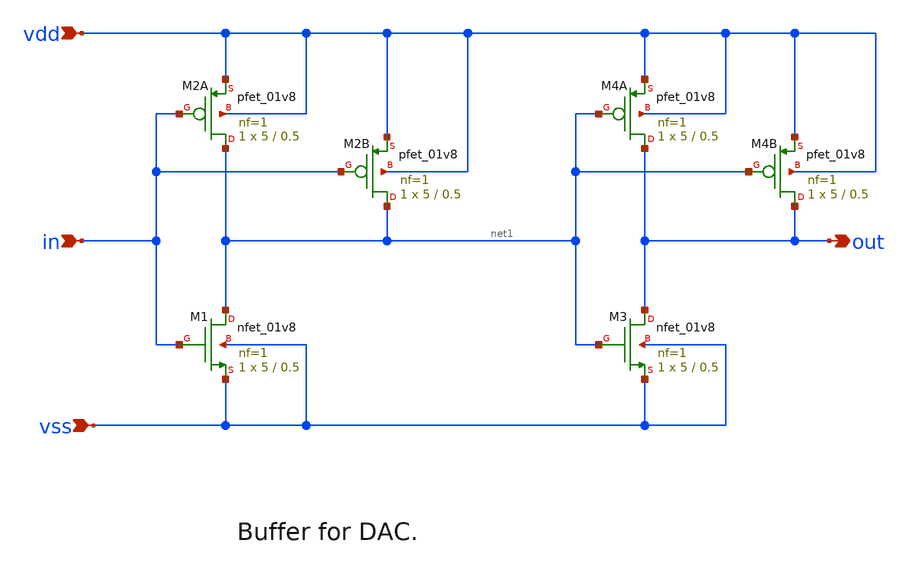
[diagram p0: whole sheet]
** sch_path: examples/3b_DAC_AMS/xschem/dac_drv.sch
**.subckt dac_drv vdd vss in out
*.ipin vdd
*.ipin vss
*.ipin in
*.opin out
XM1 net1 in vss vss sky130_fd_pr__nfet_01v8 L=0.5 W=5 nf=1 ad='int((nf+1)/2) * W/nf * 0.29' as='int((nf+2)/2) * W/nf * 0.29'
+ pd='2*int((nf+1)/2) * (W/nf + 0.29)' ps='2*int((nf+2)/2) * (W/nf + 0.29)' nrd='0.29 / W' nrs='0.29 / W'
+ sa=0 sb=0 sd=0 mult=1 m=1
XM2A net1 in vdd vdd sky130_fd_pr__pfet_01v8 L=0.5 W=5 nf=1 ad='int((nf+1)/2) * W/nf * 0.29' as='int((nf+2)/2) * W/nf * 0.29'
+ pd='2*int((nf+1)/2) * (W/nf + 0.29)' ps='2*int((nf+2)/2) * (W/nf + 0.29)' nrd='0.29 / W' nrs='0.29 / W'
+ sa=0 sb=0 sd=0 mult=1 m=1
XM4A out net1 vdd vdd sky130_fd_pr__pfet_01v8 L=0.5 W=5 nf=1 ad='int((nf+1)/2) * W/nf * 0.29' as='int((nf+2)/2) * W/nf * 0.29'
+ pd='2*int((nf+1)/2) * (W/nf + 0.29)' ps='2*int((nf+2)/2) * (W/nf + 0.29)' nrd='0.29 / W' nrs='0.29 / W'
+ sa=0 sb=0 sd=0 mult=1 m=1
XM3 out net1 vss vss sky130_fd_pr__nfet_01v8 L=0.5 W=5 nf=1 ad='int((nf+1)/2) * W/nf * 0.29' as='int((nf+2)/2) * W/nf * 0.29'
+ pd='2*int((nf+1)/2) * (W/nf + 0.29)' ps='2*int((nf+2)/2) * (W/nf + 0.29)' nrd='0.29 / W' nrs='0.29 / W'
+ sa=0 sb=0 sd=0 mult=1 m=1
XM2B net1 in vdd vdd sky130_fd_pr__pfet_01v8 L=0.5 W=5 nf=1 ad='int((nf+1)/2) * W/nf * 0.29' as='int((nf+2)/2) * W/nf * 0.29'
+ pd='2*int((nf+1)/2) * (W/nf + 0.29)' ps='2*int((nf+2)/2) * (W/nf + 0.29)' nrd='0.29 / W' nrs='0.29 / W'
+ sa=0 sb=0 sd=0 mult=1 m=1
XM4B out net1 vdd vdd sky130_fd_pr__pfet_01v8 L=0.5 W=5 nf=1 ad='int((nf+1)/2) * W/nf * 0.29' as='int((nf+2)/2) * W/nf * 0.29'
+ pd='2*int((nf+1)/2) * (W/nf + 0.29)' ps='2*int((nf+2)/2) * (W/nf + 0.29)' nrd='0.29 / W' nrs='0.29 / W'
+ sa=0 sb=0 sd=0 mult=1 m=1
**.ends
.end
